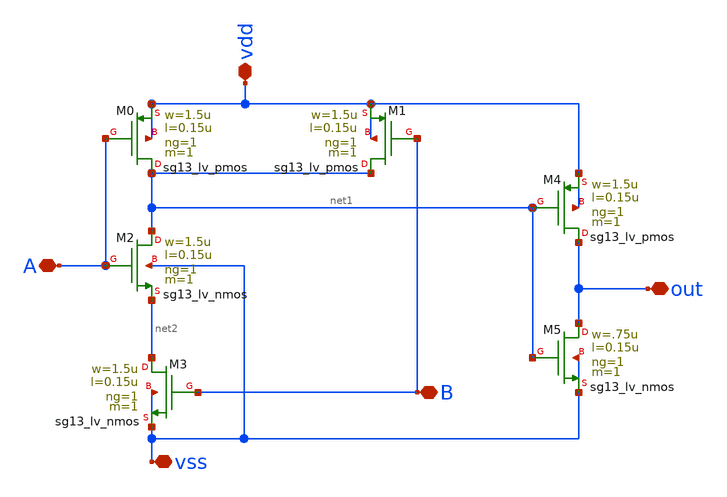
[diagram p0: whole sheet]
** sch_path: design/blocks/and2/schematic/and2.sch
**.subckt and2 A B vss vdd out
*.iopin A
*.iopin B
*.iopin vss
*.iopin vdd
*.iopin out
XM0 net1 A vdd vdd sg13_lv_pmos w=1.5u l=0.15u ng=1 m=1 mm_ok=1
XM3 net2 B vss vss sg13_lv_nmos w=1.5u l=0.15u ng=1 m=1 mm_ok=1
XM1 net1 B vdd vdd sg13_lv_pmos w=1.5u l=0.15u ng=1 m=1 mm_ok=1
XM4 out net1 vdd vdd sg13_lv_pmos w=1.5u l=0.15u ng=1 m=1 mm_ok=1
XM5 out net1 vss vss sg13_lv_nmos w=.75u l=0.15u ng=1 m=1 mm_ok=1
XM2 net1 A net2 vss sg13_lv_nmos w=1.5u l=0.15u ng=1 m=1 mm_ok=1
**.ends
.end
